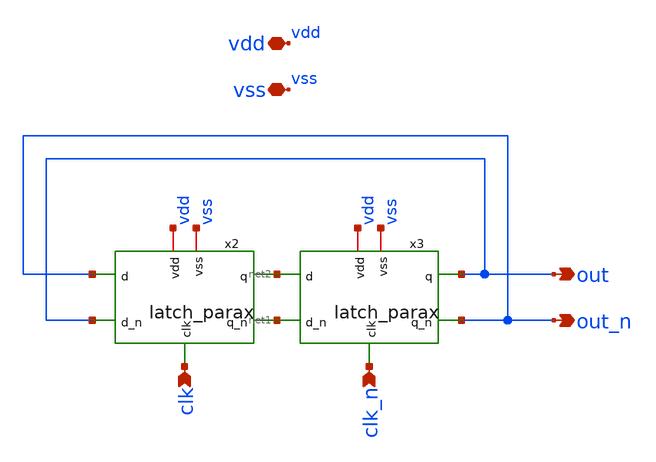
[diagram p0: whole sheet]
** sch_path: xschem/clkdiv2.sch
**.subckt clkdiv2 vdd out vss clk out_n clk_n
*.iopin vdd
*.opin out
*.iopin vss
*.ipin clk
*.opin out_n
*.ipin clk_n
x2 vdd vss net1 net2 out_n out clk latch_parax
x3 vdd vss out_n out net2 net1 clk_n latch_parax
**.ends

* expanding   symbol:  latch_parax.sym # of pins=7
** sym_path: xschem/latch.sym
.include [file normalize ../mag/latch.sim.spice]
.end
